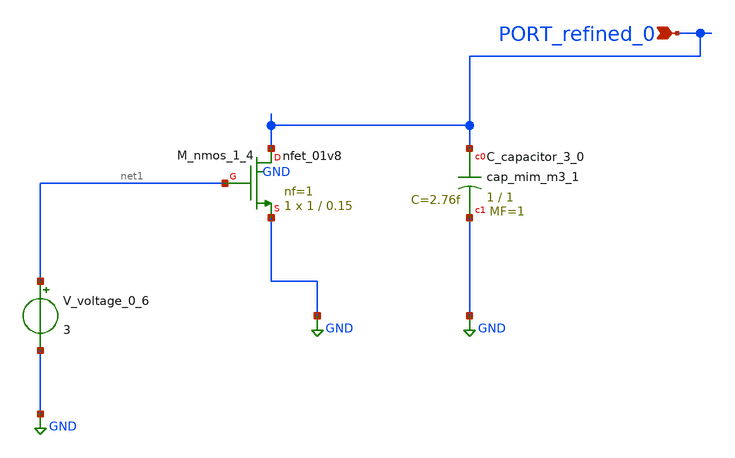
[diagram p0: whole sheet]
** sch_path: schematics/AMSNet/50.sch
**.subckt 50 PORT_refined_0
*.ipin PORT_refined_0
XC_capacitor_3_0 PORT_refined_0 GND sky130_fd_pr__cap_mim_m3_1 W=1 L=1 MF=1 m=1
XM_nmos_1_4 PORT_refined_0 net1 GND GND sky130_fd_pr__nfet_01v8 L=0.15 W=1 nf=1 ad='int((1 + 1)/2) * 1 / 1 * 0.29'
+ as='int((1 + 2)/2) * 1 / 1 * 0.29' pd='2*int((1 + 1)/2) * (1 / 1 + 0.29)' ps='2*int((1 + 2)/2) * (1 / 1 + 0.29)'
+ nrd='0.29 / 1 ' nrs='0.29 / 1 ' sa=0 sb=0 sd=0 mult=1 m=1
V_voltage_0_6 net1 GND 3
**.ends
.GLOBAL GND
.end
